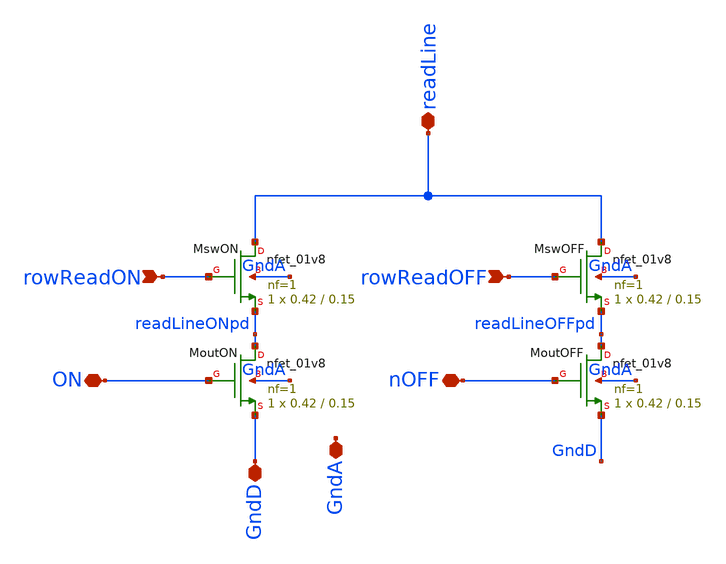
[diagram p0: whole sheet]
** sch_path: analog/klayout/production/final_merge_20260923/testbenches/cace/analog/xschem/PixelHandshake.sch
**.subckt PixelHandshake rowReadON rowReadOFF readLine ON nOFF GndD GndA
*.ipin rowReadON
*.ipin rowReadOFF
*.iopin readLine
*.iopin ON
*.iopin nOFF
*.iopin GndD
*.iopin GndA
XMswON readLine rowReadON readLineONpd GndA sky130_fd_pr__nfet_01v8 L=0.15 W=0.42 nf=1 ad='int((1 + 1)/2) * 0.42 / 1 * 0.29'
+ as='int((1 + 2)/2) * 0.42 / 1 * 0.29' pd='2*int((1 + 1)/2) * (0.42 / 1 + 0.29)' ps='2*int((1 + 2)/2) * (0.42 / 1 + 0.29)'
+ nrd='0.29 / 0.42 ' nrs='0.29 / 0.42 ' sa=0 sb=0 sd=0 mult=1 m=1
XMoutON readLineONpd ON GndD GndA sky130_fd_pr__nfet_01v8 L=0.15 W=0.42 nf=1 ad='int((1 + 1)/2) * 0.42 / 1 * 0.29'
+ as='int((1 + 2)/2) * 0.42 / 1 * 0.29' pd='2*int((1 + 1)/2) * (0.42 / 1 + 0.29)' ps='2*int((1 + 2)/2) * (0.42 / 1 + 0.29)'
+ nrd='0.29 / 0.42 ' nrs='0.29 / 0.42 ' sa=0 sb=0 sd=0 mult=1 m=1
XMswOFF readLine rowReadOFF readLineOFFpd GndA sky130_fd_pr__nfet_01v8 L=0.15 W=0.42 nf=1 ad='int((1 + 1)/2) * 0.42 / 1 * 0.29'
+ as='int((1 + 2)/2) * 0.42 / 1 * 0.29' pd='2*int((1 + 1)/2) * (0.42 / 1 + 0.29)' ps='2*int((1 + 2)/2) * (0.42 / 1 + 0.29)'
+ nrd='0.29 / 0.42 ' nrs='0.29 / 0.42 ' sa=0 sb=0 sd=0 mult=1 m=1
XMoutOFF readLineOFFpd nOFF GndD GndA sky130_fd_pr__nfet_01v8 L=0.15 W=0.42 nf=1 ad='int((1 + 1)/2) * 0.42 / 1 * 0.29'
+ as='int((1 + 2)/2) * 0.42 / 1 * 0.29' pd='2*int((1 + 1)/2) * (0.42 / 1 + 0.29)' ps='2*int((1 + 2)/2) * (0.42 / 1 + 0.29)'
+ nrd='0.29 / 0.42 ' nrs='0.29 / 0.42 ' sa=0 sb=0 sd=0 mult=1 m=1
**.ends
.end
